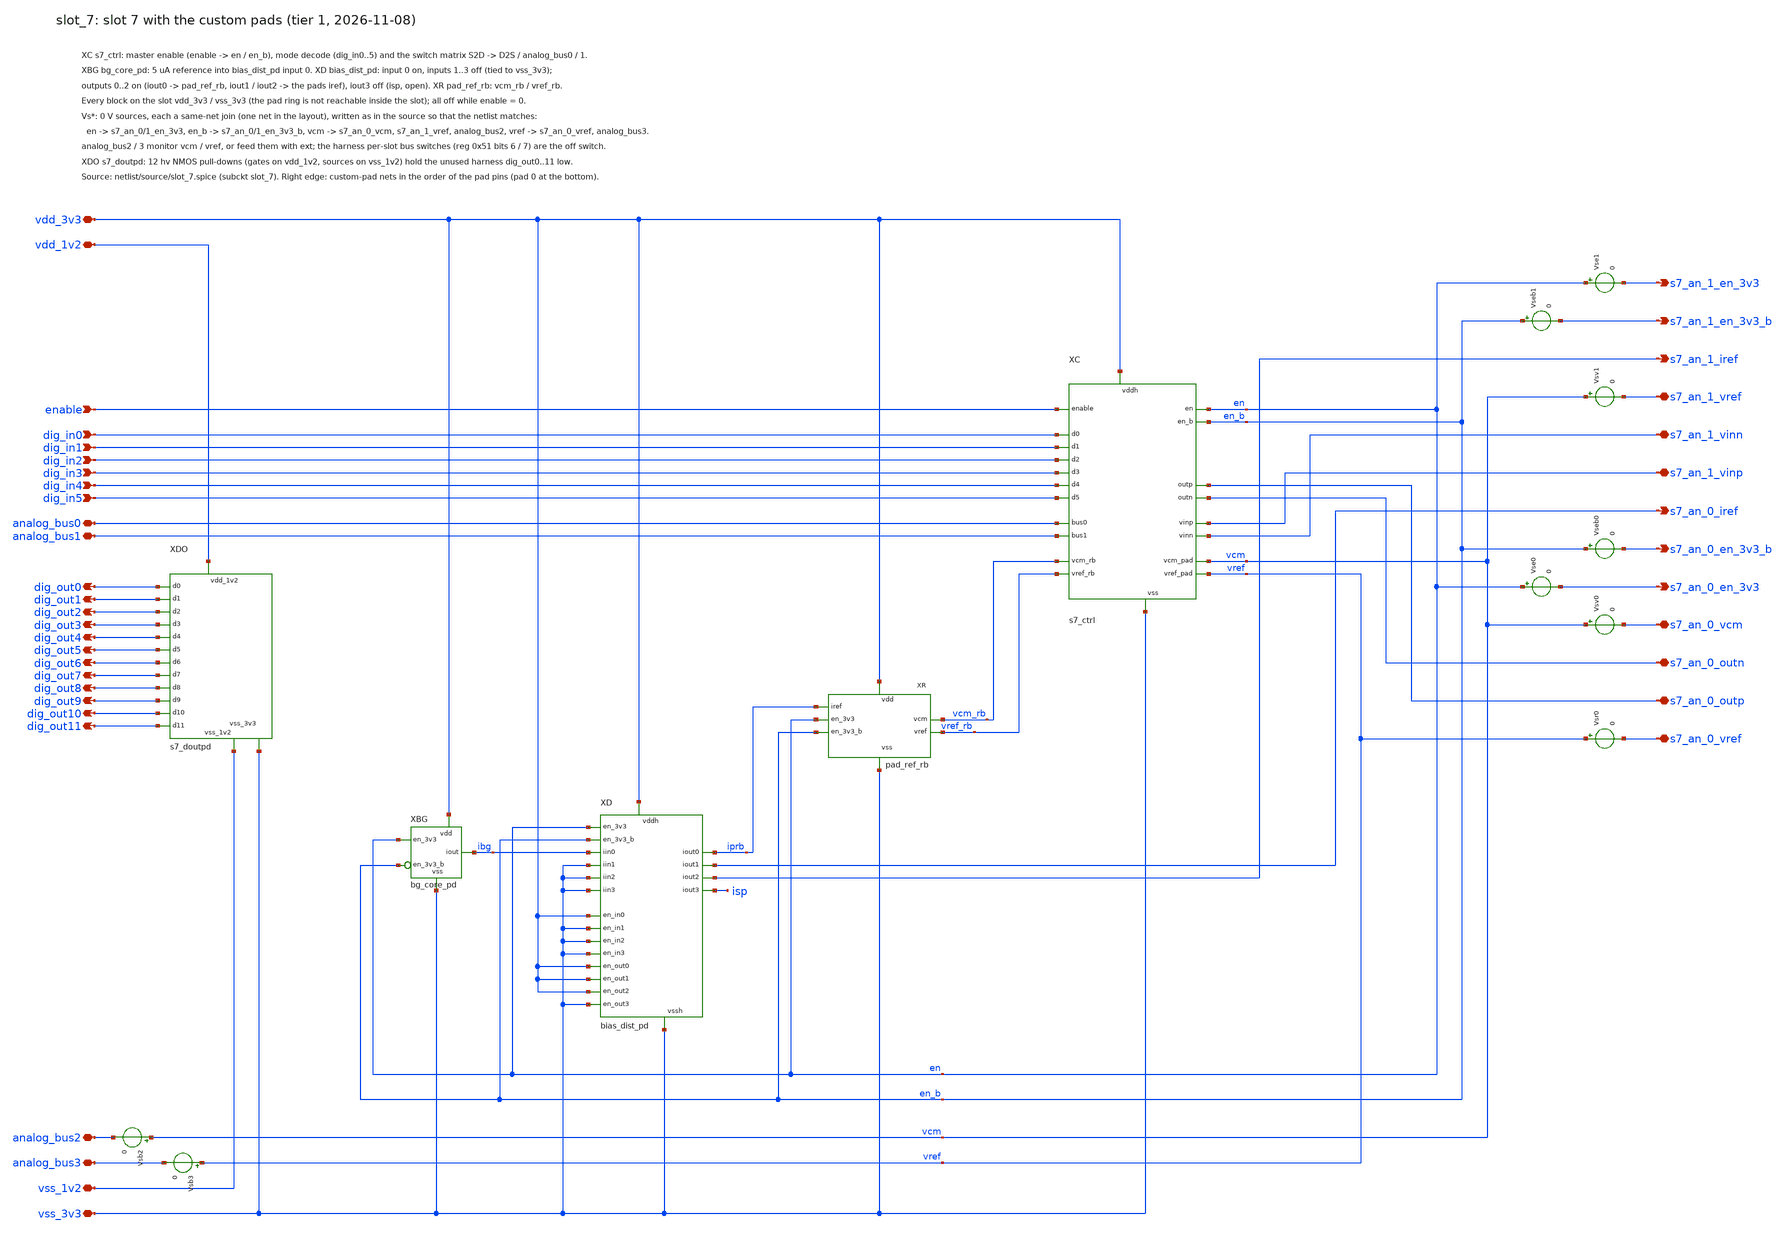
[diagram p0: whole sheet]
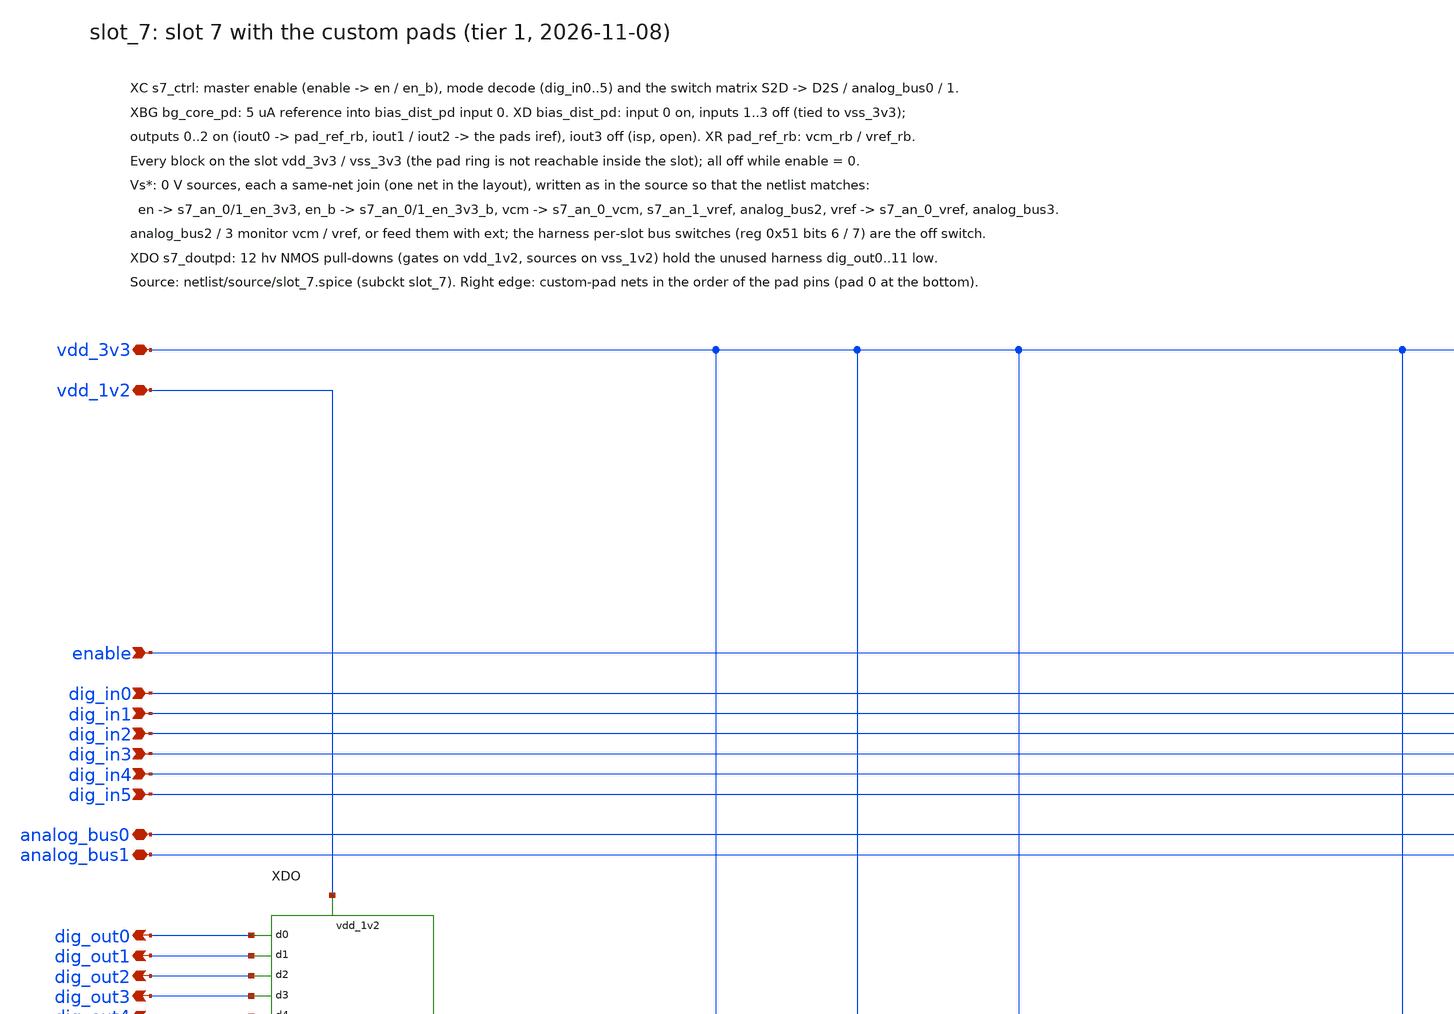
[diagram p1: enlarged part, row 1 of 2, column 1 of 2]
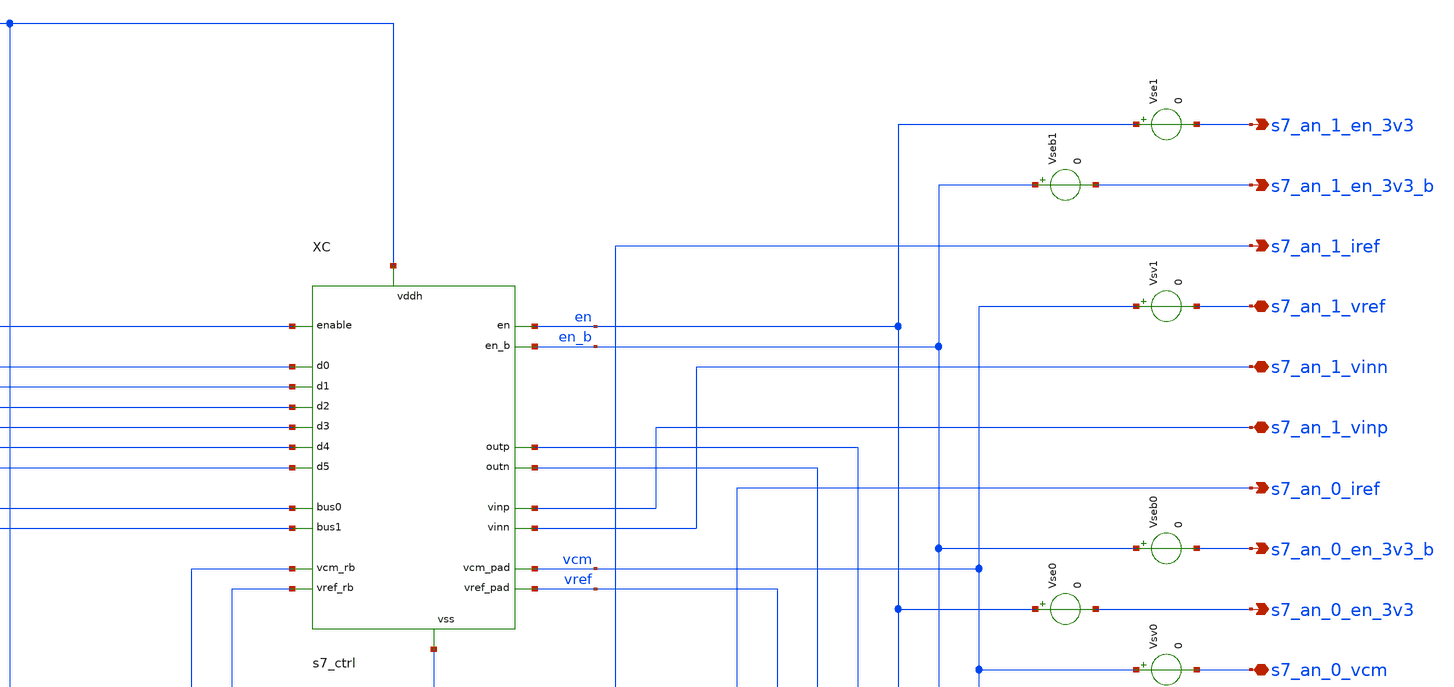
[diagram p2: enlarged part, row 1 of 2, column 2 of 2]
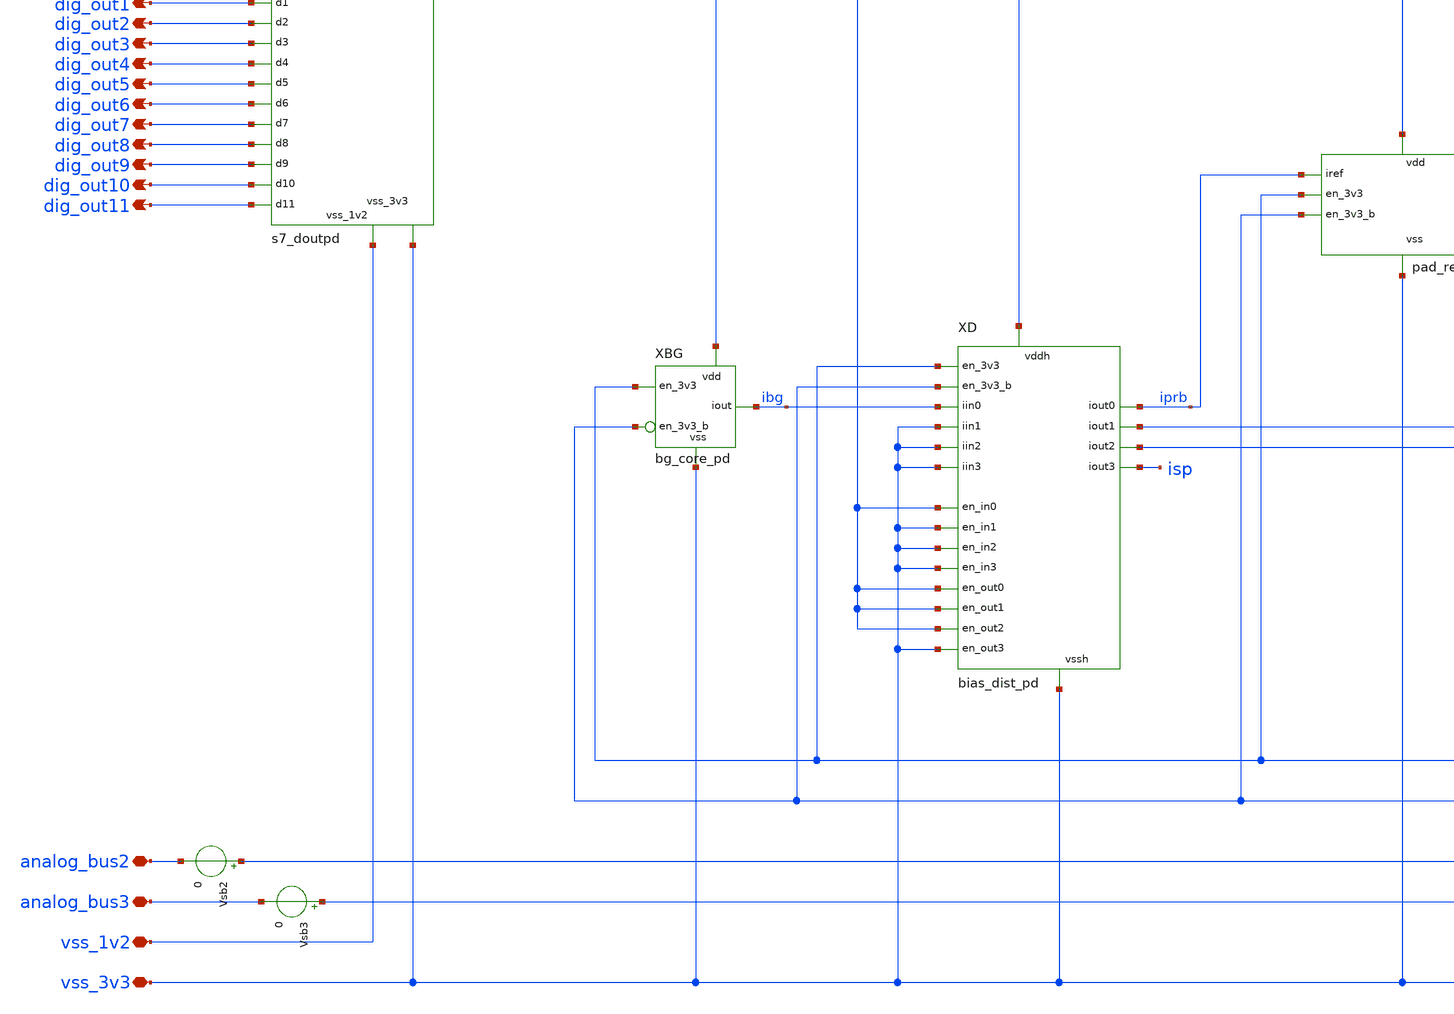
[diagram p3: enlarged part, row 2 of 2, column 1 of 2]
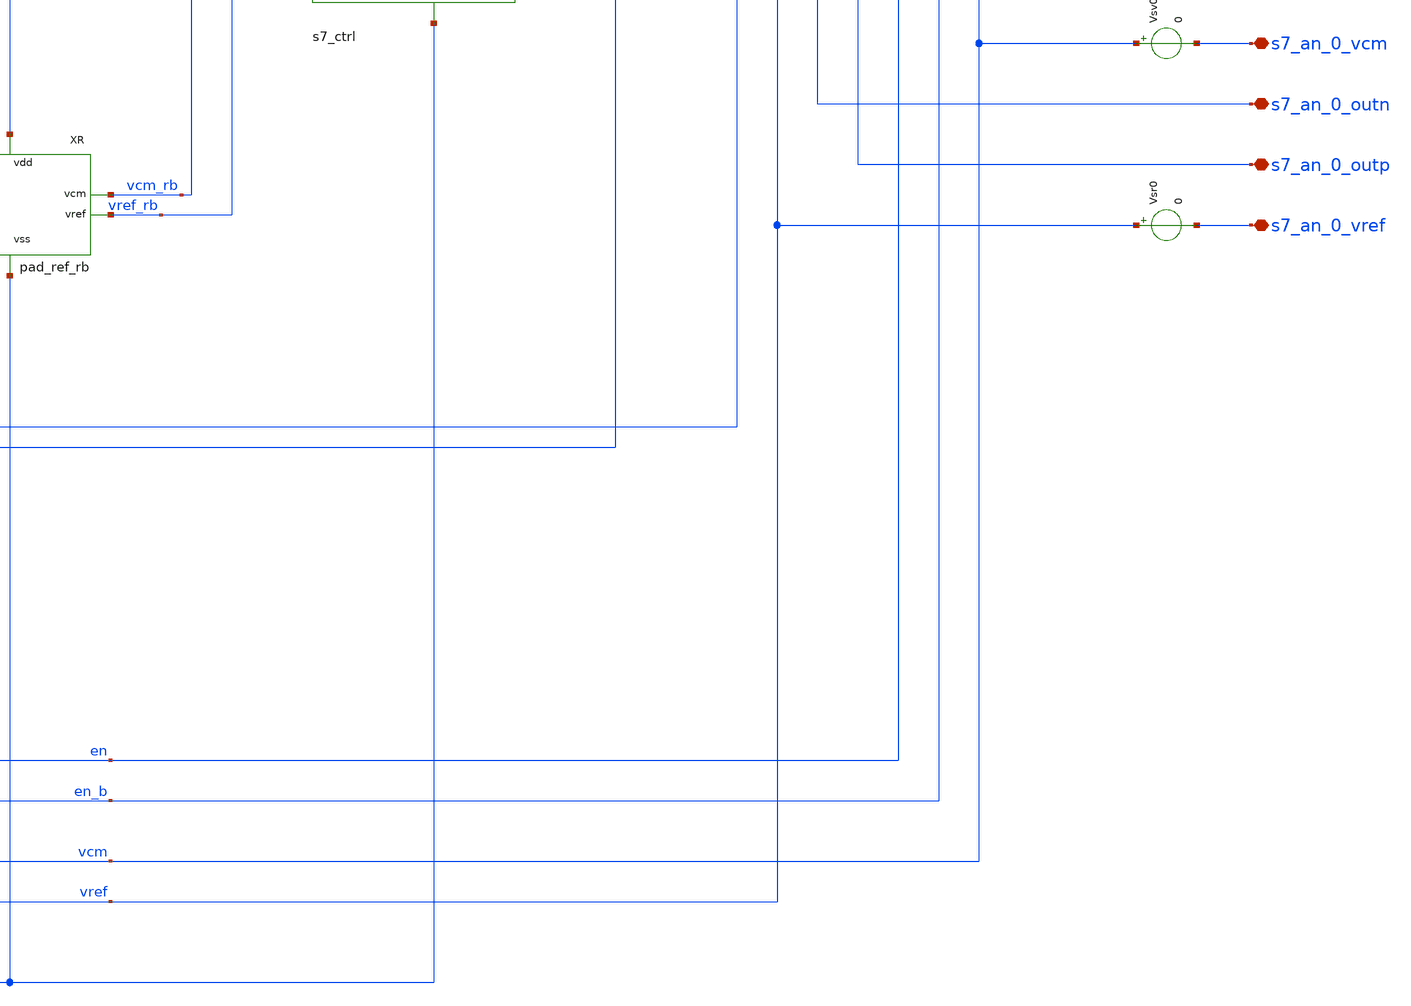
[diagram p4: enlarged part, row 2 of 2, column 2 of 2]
** sch_path: macros/slot_7/schematic/xschem/slot_7.sch
**.subckt slot_7 vdd_3v3 vss_3v3 enable dig_in0 dig_in1 dig_in2 dig_in3 dig_in4 dig_in5 analog_bus0
*+ analog_bus1 analog_bus2 analog_bus3 s7_an_0_vref s7_an_0_outp s7_an_0_outn s7_an_0_vcm s7_an_0_en_3v3
*+ s7_an_0_en_3v3_b s7_an_0_iref s7_an_1_vinp s7_an_1_vinn s7_an_1_vref s7_an_1_iref s7_an_1_en_3v3_b s7_an_1_en_3v3
*+ dig_out0 dig_out1 dig_out2 dig_out3 dig_out4 dig_out5 dig_out6 dig_out7 dig_out8 dig_out9 dig_out10
*+ dig_out11 vdd_1v2 vss_1v2
*.iopin vdd_3v3
*.iopin vss_3v3
*.ipin enable
*.ipin dig_in0
*.ipin dig_in1
*.ipin dig_in2
*.ipin dig_in3
*.ipin dig_in4
*.ipin dig_in5
*.iopin analog_bus0
*.iopin analog_bus1
*.iopin analog_bus2
*.iopin analog_bus3
*.iopin s7_an_0_vref
*.iopin s7_an_0_outp
*.iopin s7_an_0_outn
*.iopin s7_an_0_vcm
*.opin s7_an_0_en_3v3
*.opin s7_an_0_en_3v3_b
*.opin s7_an_0_iref
*.iopin s7_an_1_vinp
*.iopin s7_an_1_vinn
*.iopin s7_an_1_vref
*.opin s7_an_1_iref
*.opin s7_an_1_en_3v3_b
*.opin s7_an_1_en_3v3
*.opin dig_out0
*.opin dig_out1
*.opin dig_out2
*.opin dig_out3
*.opin dig_out4
*.opin dig_out5
*.opin dig_out6
*.opin dig_out7
*.opin dig_out8
*.opin dig_out9
*.opin dig_out10
*.opin dig_out11
*.iopin vdd_1v2
*.iopin vss_1v2
XC vdd_3v3 vss_3v3 enable dig_in0 dig_in1 dig_in2 dig_in3 dig_in4 dig_in5 en en_b s7_an_0_outp
+ s7_an_0_outn s7_an_1_vinp s7_an_1_vinn analog_bus0 analog_bus1 vcm_rb vref_rb vcm vref s7_ctrl
XBG vdd_3v3 vss_3v3 ibg en en_b bg_core_pd
XD vdd_3v3 vss_3v3 en en_b ibg vss_3v3 vss_3v3 vss_3v3 vdd_3v3 vss_3v3 vss_3v3 vss_3v3 iprb
+ s7_an_0_iref s7_an_1_iref isp vdd_3v3 vdd_3v3 vdd_3v3 vss_3v3 bias_dist_pd
XR vdd_3v3 vss_3v3 iprb vcm_rb vref_rb en en_b pad_ref_rb
XDO dig_out0 dig_out1 dig_out2 dig_out3 dig_out4 dig_out5 dig_out6 dig_out7 dig_out8 dig_out9
+ dig_out10 dig_out11 vdd_1v2 vss_1v2 vss_3v3 s7_doutpd
Vsr0 vref s7_an_0_vref 0
Vse1 en s7_an_1_en_3v3 0
Vse0 en s7_an_0_en_3v3 0
Vseb1 en_b s7_an_1_en_3v3_b 0
Vseb0 en_b s7_an_0_en_3v3_b 0
Vsv1 vcm s7_an_1_vref 0
Vsv0 vcm s7_an_0_vcm 0
Vsb2 vcm analog_bus2 0
Vsb3 vref analog_bus3 0
**.ends
.end
